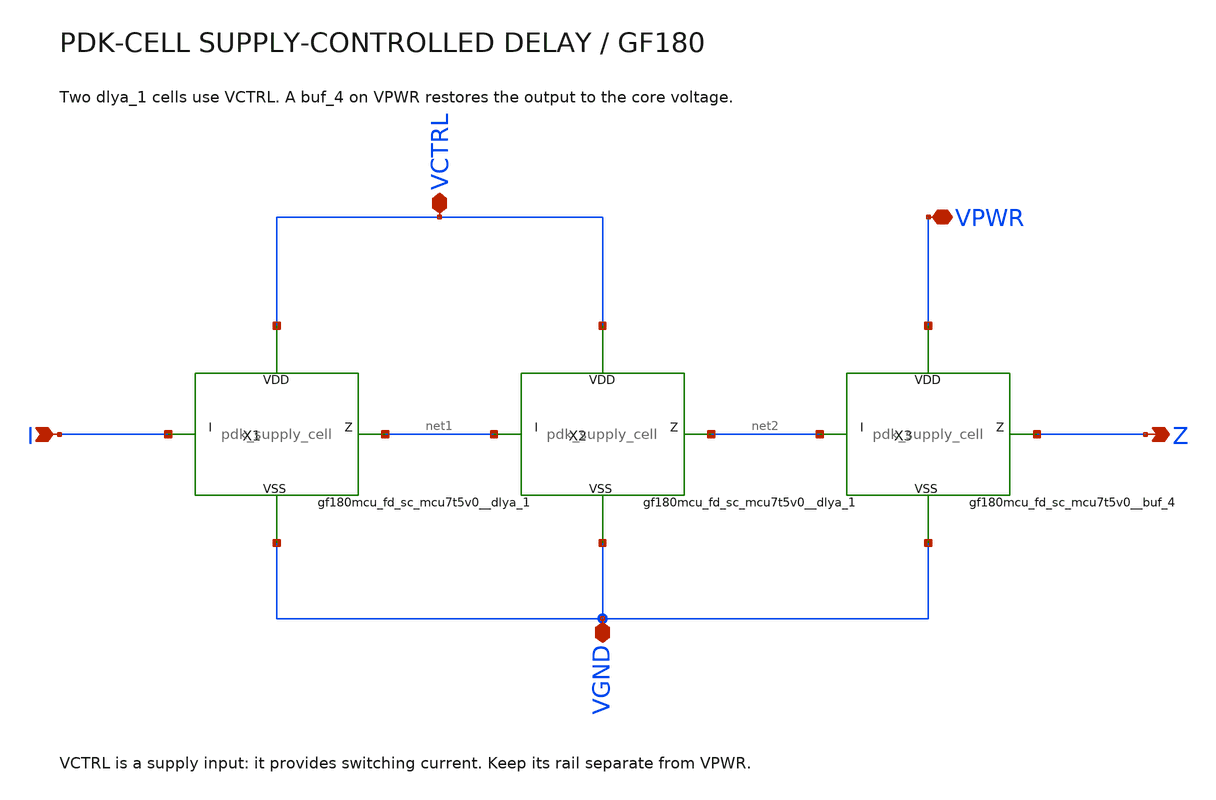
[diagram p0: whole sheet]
** sch_path: schem/tdc_vcd.sch
**.subckt tdc_vcd I Z VCTRL VPWR VGND
*.ipin I
*.opin Z
*.iopin VCTRL
*.iopin VPWR
*.iopin VGND
X1 I net1 VCTRL VCTRL VGND VGND gf180mcu_fd_sc_mcu7t5v0__dlya_1
X2 net1 net2 VCTRL VCTRL VGND VGND gf180mcu_fd_sc_mcu7t5v0__dlya_1
X3 net2 Z VPWR VPWR VGND VGND gf180mcu_fd_sc_mcu7t5v0__buf_4
**.ends
.end
